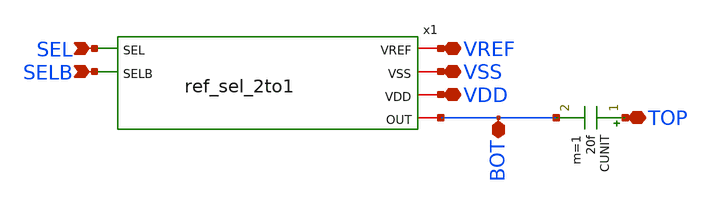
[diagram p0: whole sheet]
** sch_path: designs/libs/core_matchmaker/cdac_unit/cdac_unit_cell.sch
**.subckt cdac_unit_cell TOP VREF VSS VDD SEL SELB BOT
*.iopin TOP
*.iopin VREF
*.iopin VSS
*.iopin VDD
*.ipin SEL
*.ipin SELB
*.iopin BOT
x1 SEL VREF VSS SELB VDD BOT ref_sel_2to1
CUNIT TOP BOT 20f m=1
**.ends
.end
